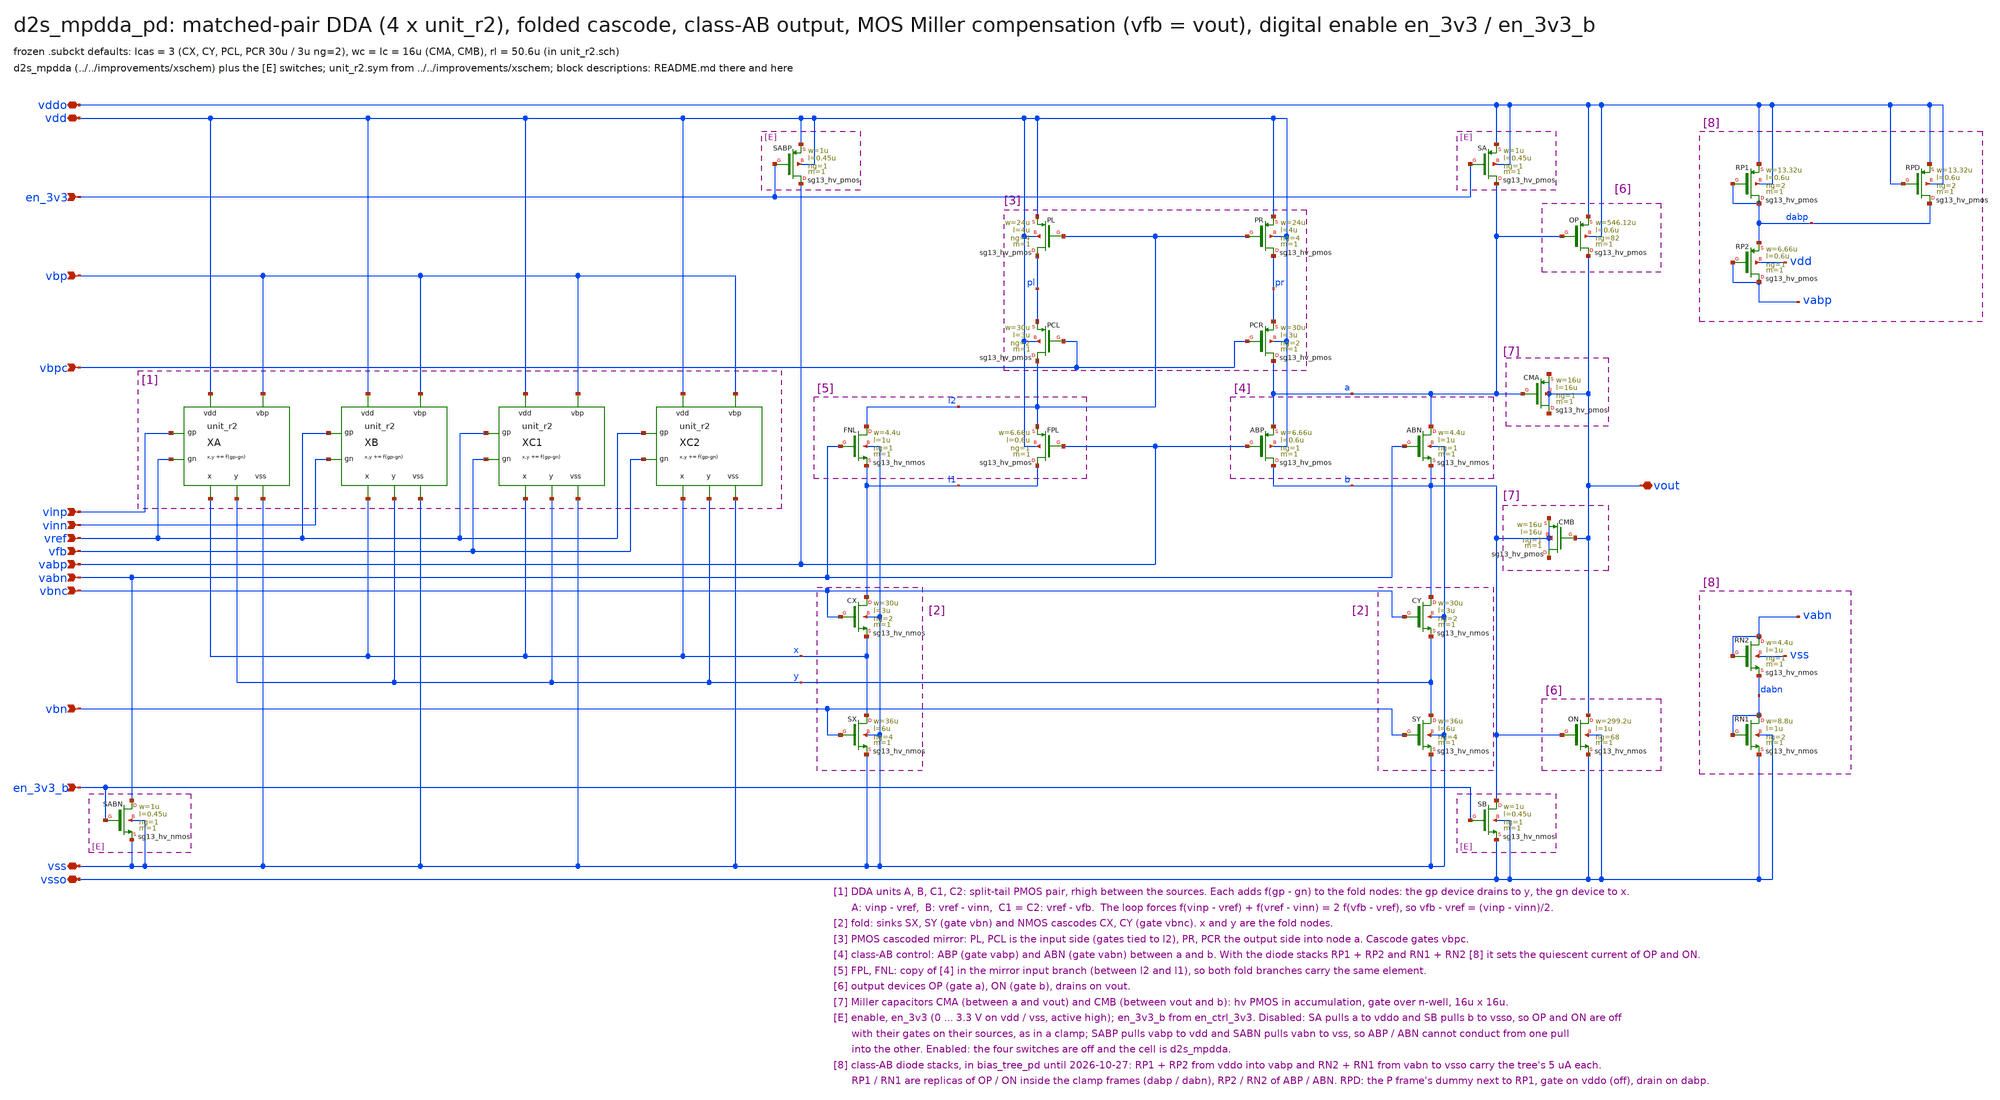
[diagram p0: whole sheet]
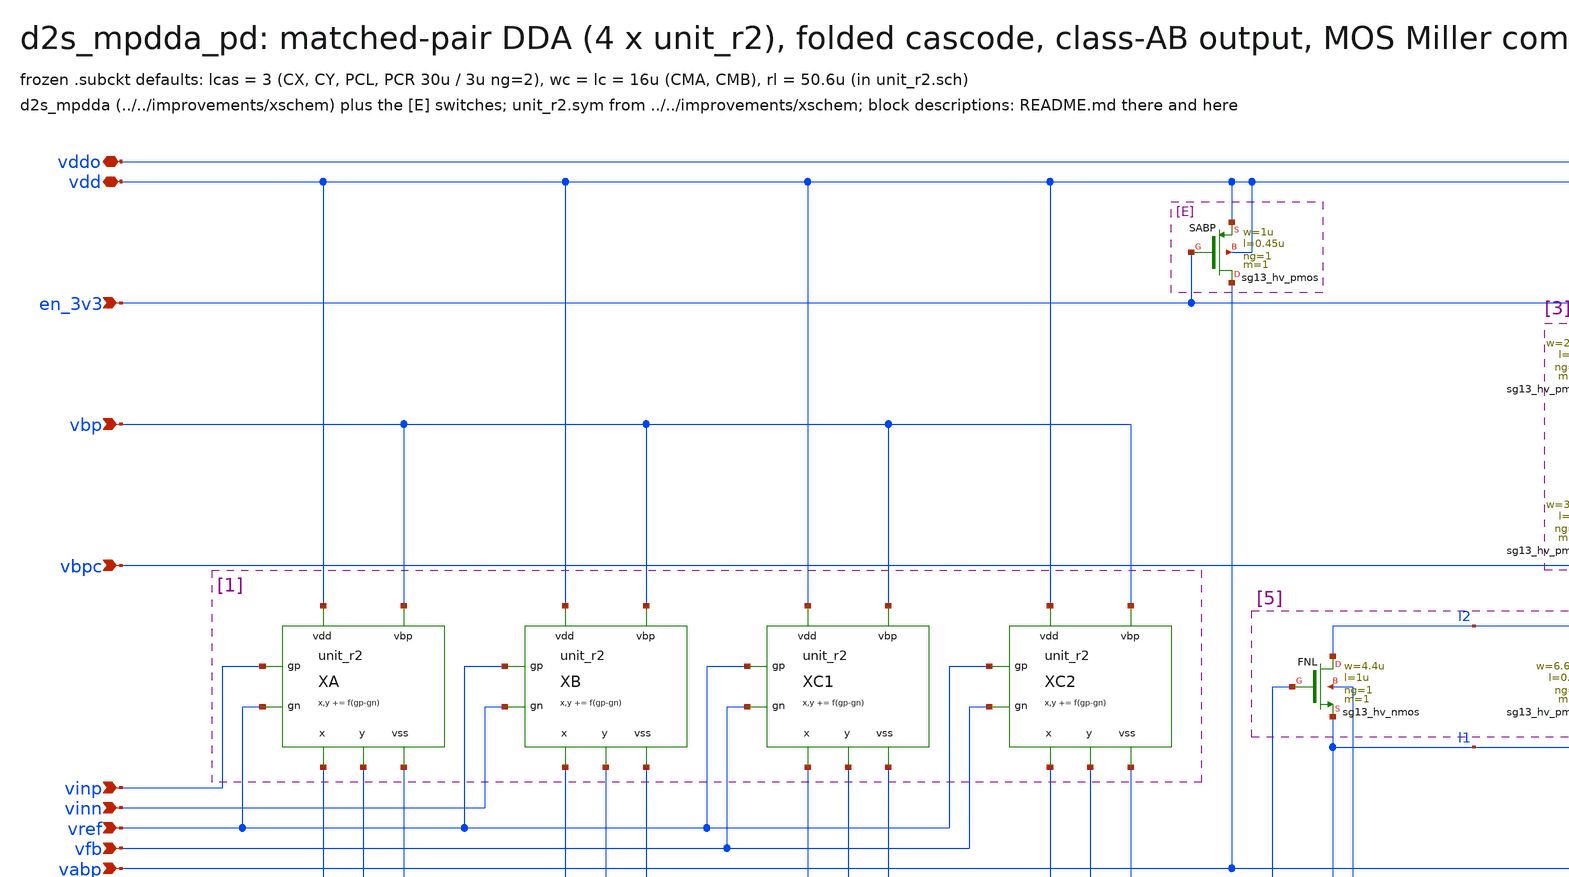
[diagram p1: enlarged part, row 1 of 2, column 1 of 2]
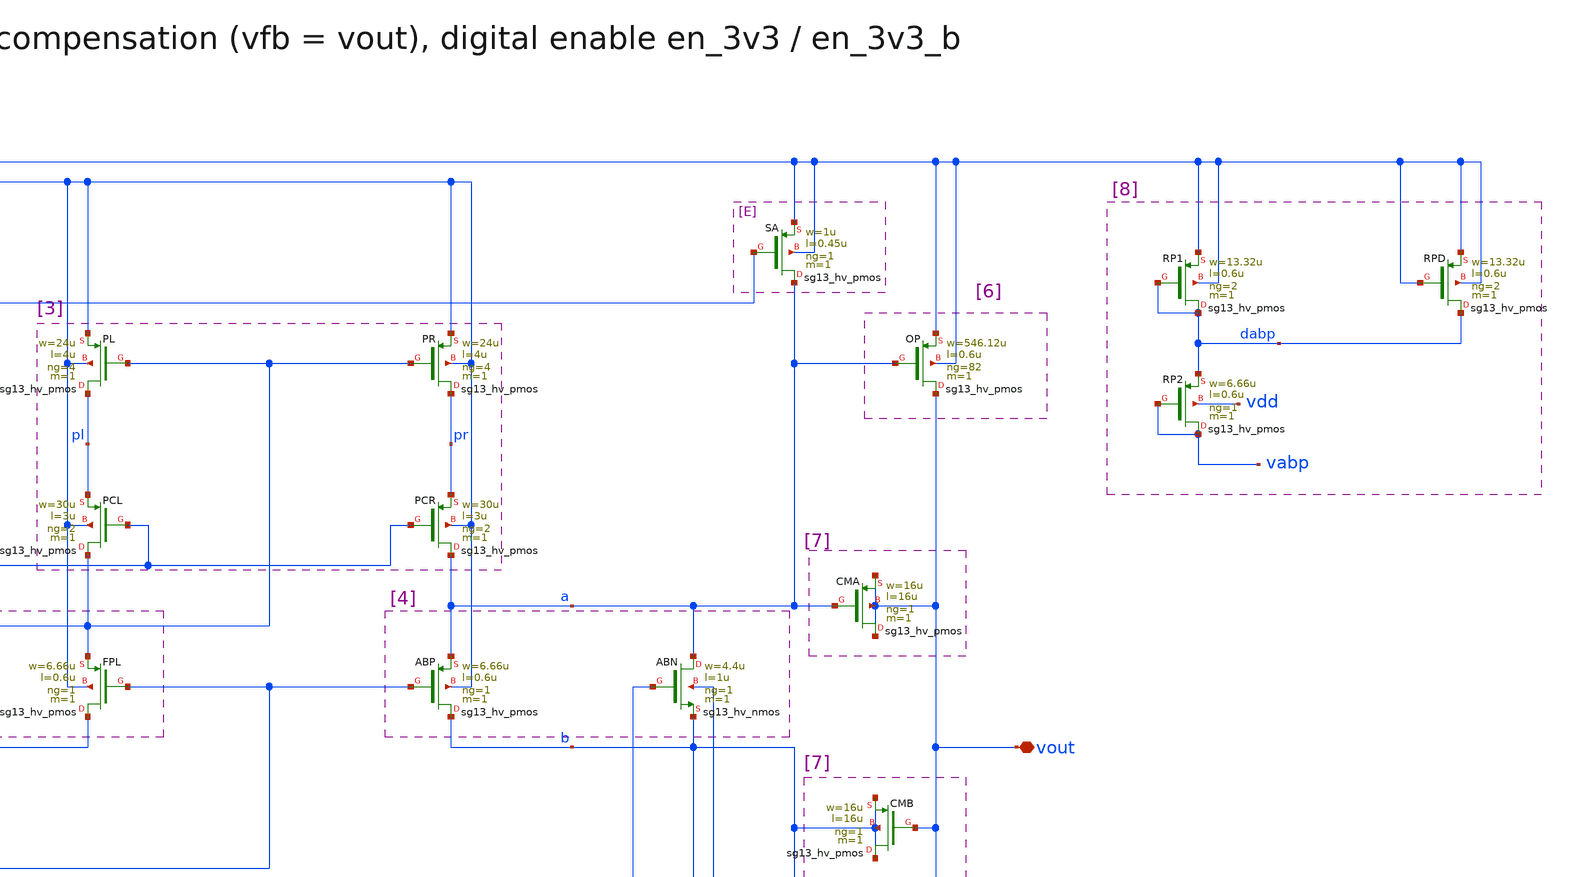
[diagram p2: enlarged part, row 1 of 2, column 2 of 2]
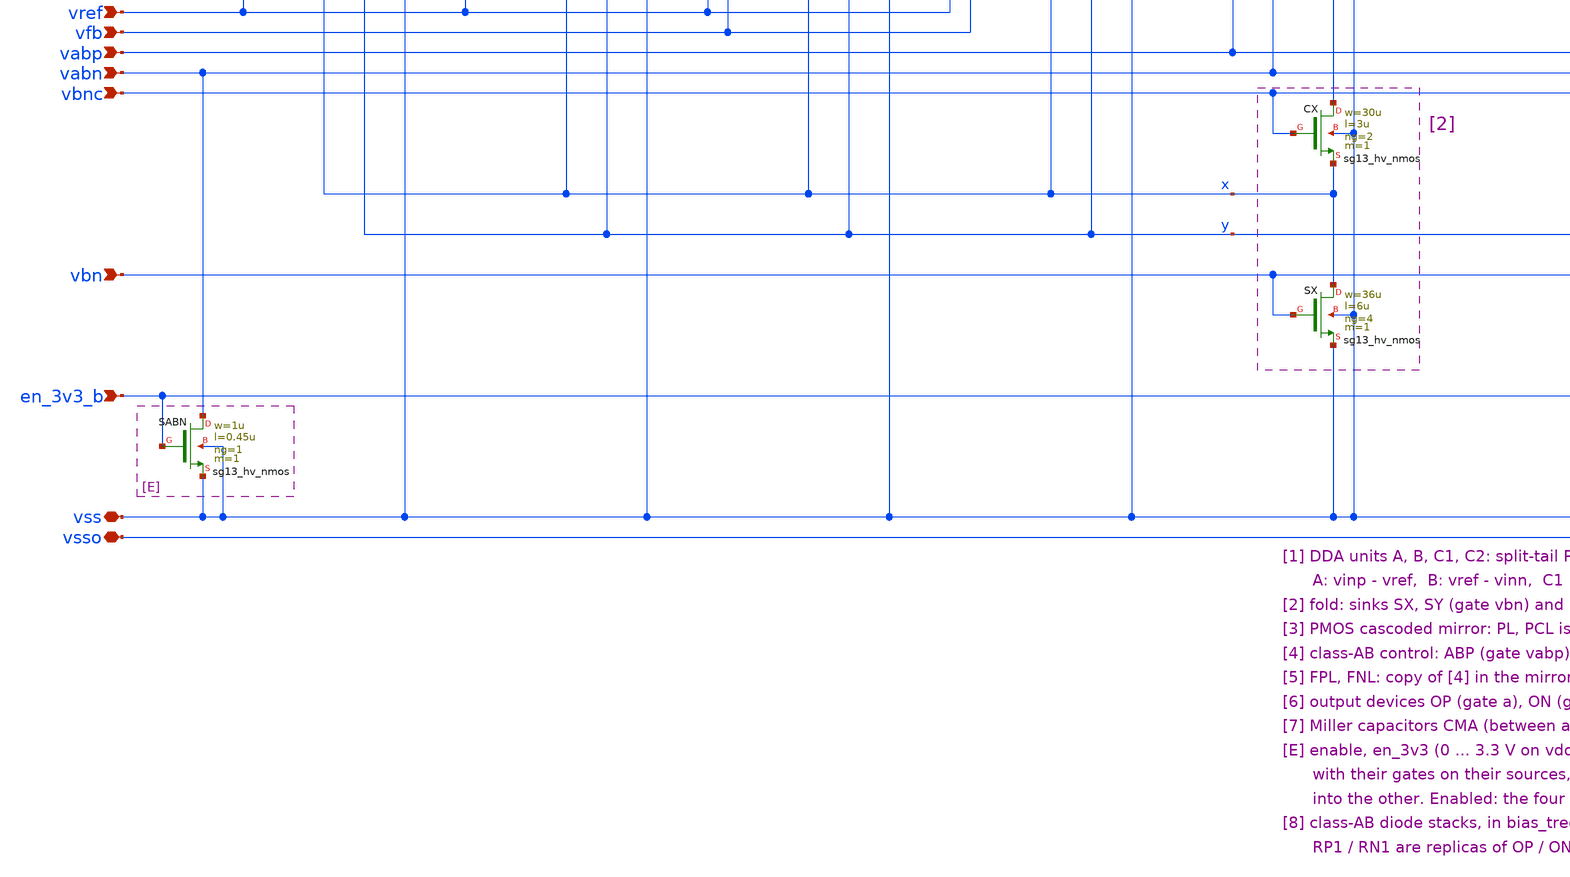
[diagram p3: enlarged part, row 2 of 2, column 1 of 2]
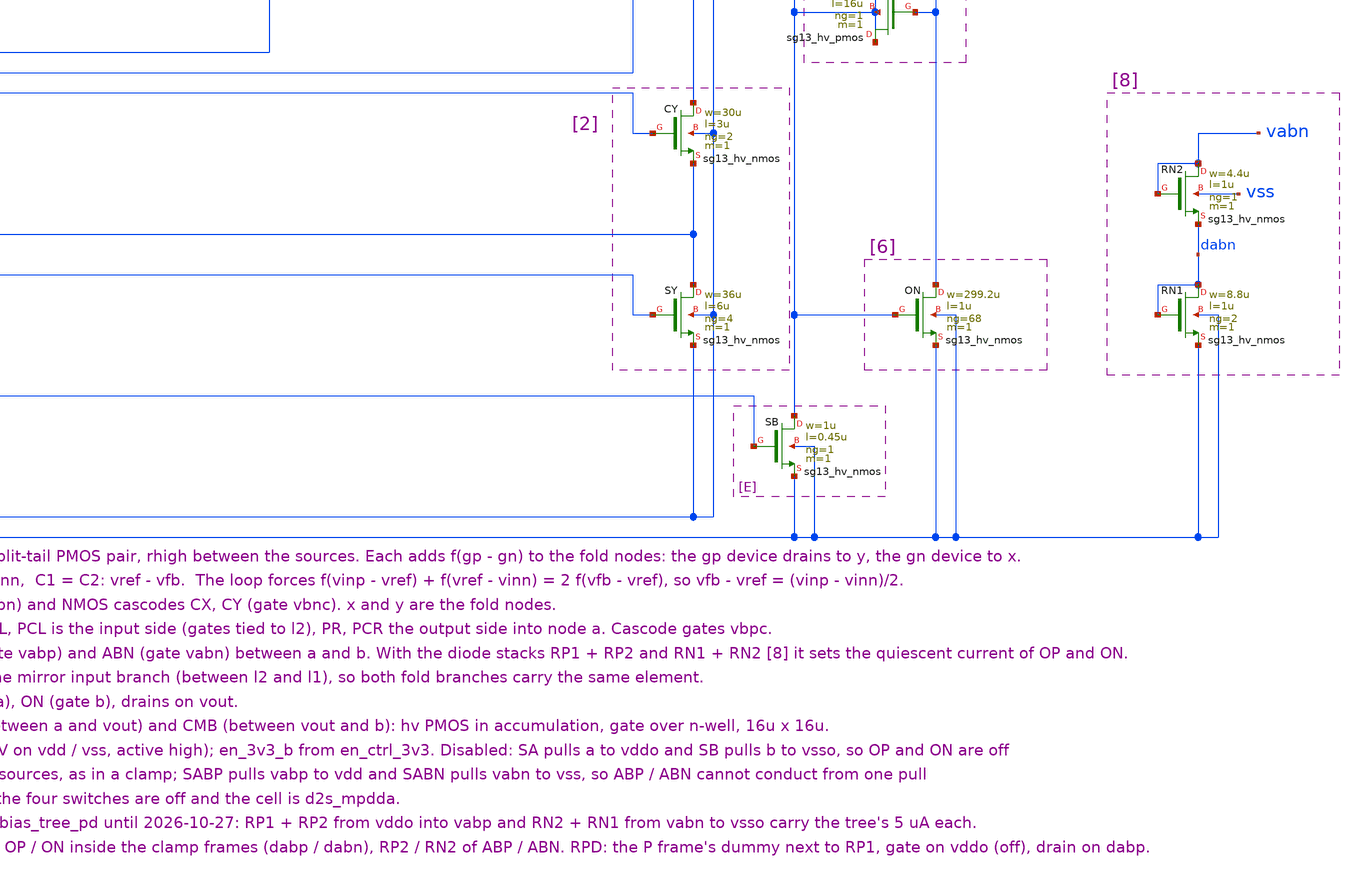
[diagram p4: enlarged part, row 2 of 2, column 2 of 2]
** sch_path: macros/sg13cmos5l_IOPadDiff2Single/schematic/xschem/d2s_mpdda_pd.sch
**.subckt d2s_mpdda_pd vdd vss vddo vsso vinp vinn vref vout vfb vbp vbn vbpc vbnc vabp vabn en_3v3
*+ en_3v3_b
*.iopin vdd
*.iopin vss
*.iopin vddo
*.iopin vsso
*.ipin vinp
*.ipin vinn
*.ipin vref
*.iopin vout
*.ipin vfb
*.ipin vbp
*.ipin vbn
*.ipin vbpc
*.ipin vbnc
*.ipin vabp
*.ipin vabn
*.ipin en_3v3
*.ipin en_3v3_b
XA x y vinp vref vdd vss vbp unit_r2
XB x y vref vinn vdd vss vbp unit_r2
XC1 x y vref vfb vdd vss vbp unit_r2
XC2 x y vref vfb vdd vss vbp unit_r2
XFNL l2 vabn l1 vss sg13_hv_nmos w=4.4u l=1u ng=1 m=1 mm_ok=1
XCX l1 vbnc x vss sg13_hv_nmos w=30u l=3u ng=2 m=1 mm_ok=1
XSX x vbn vss vss sg13_hv_nmos w=36u l=6u ng=4 m=1 mm_ok=1
XPL pl l2 vdd vdd sg13_hv_pmos w=24u l=4u ng=4 m=1 mm_ok=1
XPCL l2 vbpc pl vdd sg13_hv_pmos w=30u l=3u ng=2 m=1 mm_ok=1
XFPL l1 vabp l2 vdd sg13_hv_pmos w=6.66u l=0.6u ng=1 m=1 mm_ok=1
XPR pr l2 vdd vdd sg13_hv_pmos w=24u l=4u ng=4 m=1 mm_ok=1
XPCR a vbpc pr vdd sg13_hv_pmos w=30u l=3u ng=2 m=1 mm_ok=1
XABP b vabp a vdd sg13_hv_pmos w=6.66u l=0.6u ng=1 m=1 mm_ok=1
XABN a vabn b vss sg13_hv_nmos w=4.4u l=1u ng=1 m=1 mm_ok=1
XCY b vbnc y vss sg13_hv_nmos w=30u l=3u ng=2 m=1 mm_ok=1
XSY y vbn vss vss sg13_hv_nmos w=36u l=6u ng=4 m=1 mm_ok=1
XOP vout a vddo vddo sg13_hv_pmos w=546.12u l=0.6u ng=82 m=1 mm_ok=1
XON vout b vsso vsso sg13_hv_nmos w=299.2u l=1u ng=68 m=1 mm_ok=1
XCMA vout a vout vout sg13_hv_pmos w=16u l=16u ng=1 m=1 mm_ok=1
XCMB b vout b b sg13_hv_pmos w=16u l=16u ng=1 m=1 mm_ok=1
XSABP vabp en_3v3 vdd vdd sg13_hv_pmos w=1u l=0.45u ng=1 m=1 mm_ok=1
XSA a en_3v3 vddo vddo sg13_hv_pmos w=1u l=0.45u ng=1 m=1 mm_ok=1
XSABN vabn en_3v3_b vss vss sg13_hv_nmos w=1u l=0.45u ng=1 m=1 mm_ok=1
XSB b en_3v3_b vsso vsso sg13_hv_nmos w=1u l=0.45u ng=1 m=1 mm_ok=1
XRP1 dabp dabp vddo vddo sg13_hv_pmos w=13.32u l=0.6u ng=2 m=1 mm_ok=1
XRPD dabp vddo vddo vddo sg13_hv_pmos w=13.32u l=0.6u ng=2 m=1 mm_ok=1
XRP2 vabp vabp dabp vdd sg13_hv_pmos w=6.66u l=0.6u ng=1 m=1 mm_ok=1
XRN2 vabn vabn dabn vss sg13_hv_nmos w=4.4u l=1u ng=1 m=1 mm_ok=1
XRN1 dabn dabn vsso vsso sg13_hv_nmos w=8.8u l=1u ng=2 m=1 mm_ok=1
**.ends

* expanding   symbol:  unit_r2.sym # of pins=7
** sym_path: sudelbuecher/design_considerations/class_ab_pad_driver/improvements/xschem/unit_r2.sym
** sch_path: sudelbuecher/design_considerations/class_ab_pad_driver/improvements/xschem/unit_r2.sch
.subckt unit_r2 x y gp gn vdd vss vbp
*.opin x
*.opin y
*.ipin gp
*.ipin gn
*.iopin vdd
*.iopin vss
*.ipin vbp
XTa sa vbp vdd vdd sg13_hv_pmos w=5u l=6u ng=1 m=1 mm_ok=1
XTb sb vbp vdd vdd sg13_hv_pmos w=5u l=6u ng=1 m=1 mm_ok=1
XMa y gp sa sa sg13_hv_pmos w=20u l=1u ng=2 m=1 mm_ok=1
XMb x gn sb sb sg13_hv_pmos w=20u l=1u ng=2 m=1 mm_ok=1
XR sa sb vss rhigh w=0.5u l=50.6u m=1 b=0 mm_ok=1
.ends

.end
